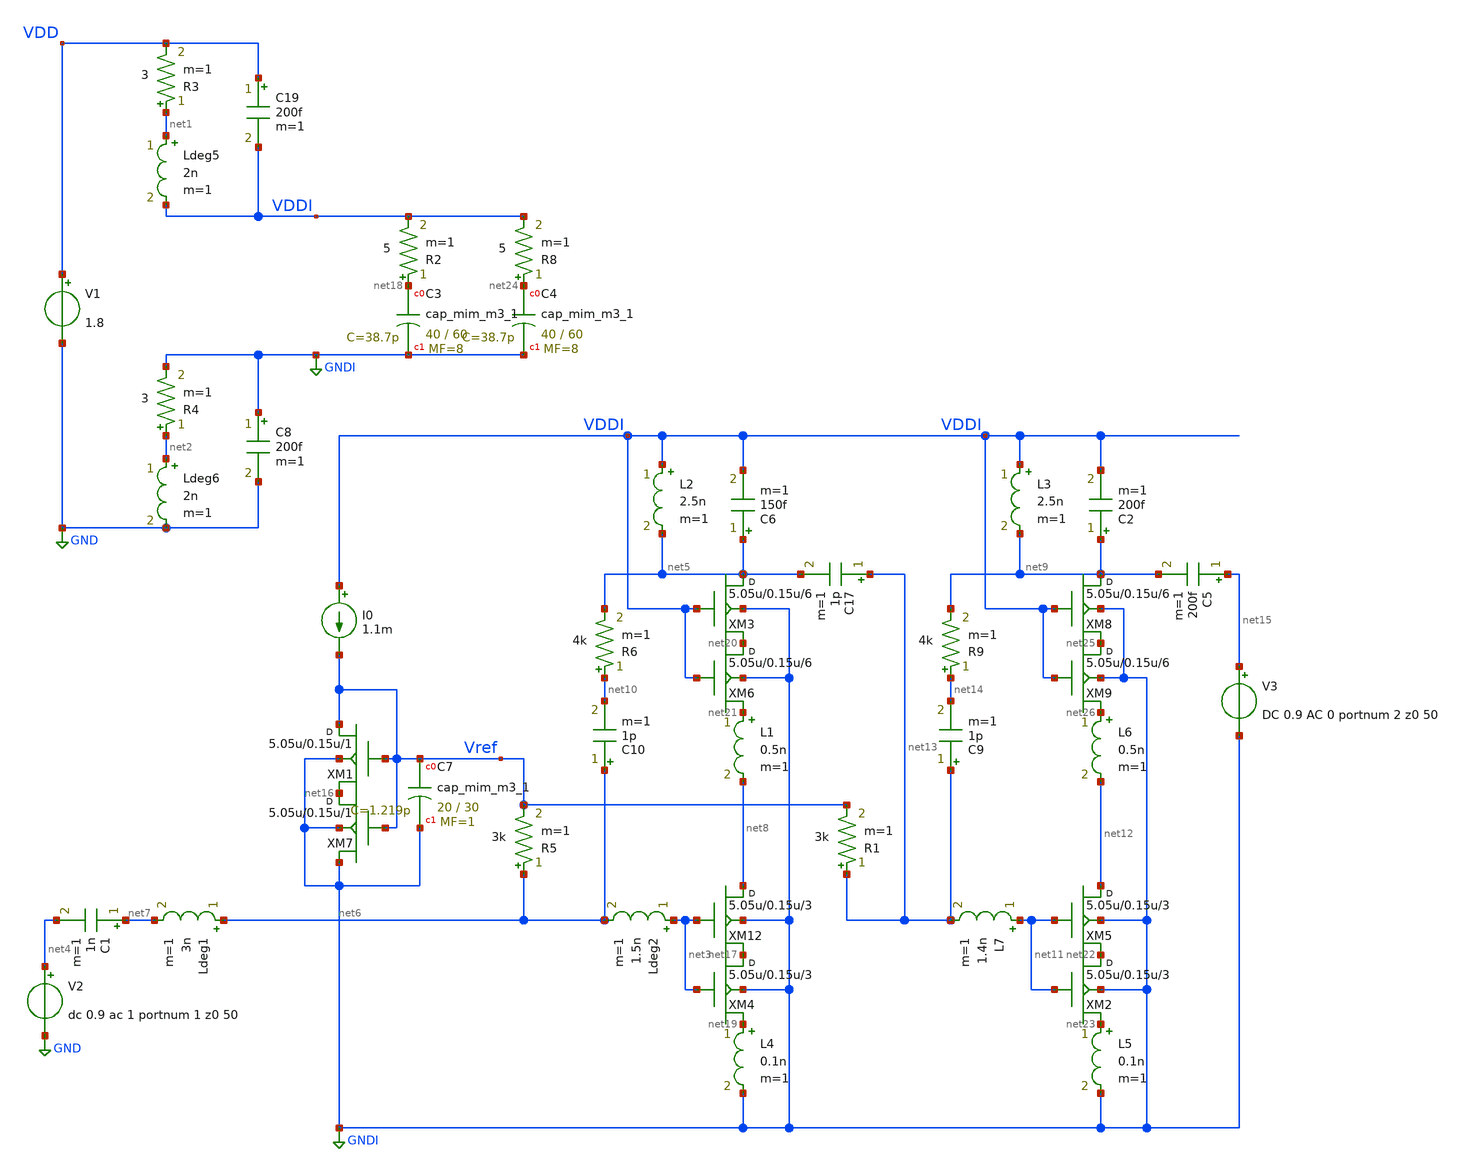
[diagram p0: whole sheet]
** sch_path: xschem/LNA5_with_output_buf_2.sch
**.subckt LNA5_with_output_buf_2
V1 VDD GND 1.8
V2 net4 GND dc 0.9 ac 1 portnum 1 z0 50
I0 VDDI Vref 1.1m
XM1 Vref Vref net16 GNDI sky130_fd_pr__rf_nfet_01v8_bM04W5p00L0p15_ext w=5.05u l=0.15u m=1
XC7 Vref GNDI sky130_fd_pr__cap_mim_m3_1 W=20 L=30 MF=1 m=1
Ldeg5 net1 VDDI 2n m=1
R3 net1 VDD 3 m=1
Ldeg6 net2 GND 2n m=1
R4 net2 GNDI 3 m=1
XM12 net8 net3 net17 GNDI sky130_fd_pr__rf_nfet_01v8_bM04W5p00L0p15_ext w=5.05u l=0.15u m=3
C17 net13 net5 1p m=1
L2 VDDI net5 2.5n m=1
XC3 net18 GNDI sky130_fd_pr__cap_mim_m3_1 W=40 L=60 MF=8 m=8
C8 GNDI GND 200f m=1
C19 VDD VDDI 200f m=1
R2 net18 VDDI 5 m=1
R5 net6 Vref 3k m=1
XM4 net17 net3 net19 GNDI sky130_fd_pr__rf_nfet_01v8_bM04W5p00L0p15_ext w=5.05u l=0.15u m=3
C1 net7 net4 1n m=1
C6 net5 VDDI 150f m=1
R6 net10 net5 4k m=1
XM3 net5 VDDI net20 GNDI sky130_fd_pr__rf_nfet_01v8_bM04W5p00L0p15_ext w=5.05u l=0.15u m=6
XM6 net20 VDDI net21 GNDI sky130_fd_pr__rf_nfet_01v8_bM04W5p00L0p15_ext w=5.05u l=0.15u m=6
XM7 net16 Vref GNDI GNDI sky130_fd_pr__rf_nfet_01v8_bM04W5p00L0p15_ext w=5.05u l=0.15u m=1
Ldeg1 net6 net7 3n m=1
L1 net21 net8 0.5n m=1
Ldeg2 net3 net6 1.5n m=1
XM2 net22 net11 net23 GNDI sky130_fd_pr__rf_nfet_01v8_bM04W5p00L0p15_ext w=5.05u l=0.15u m=3
V3 net15 GNDI DC 0.9 AC 0 portnum 2 z0 50
L5 net23 GNDI 0.1n m=1
L7 net11 net13 1.4n m=1
R1 net13 Vref 3k m=1
XM5 net12 net11 net22 GNDI sky130_fd_pr__rf_nfet_01v8_bM04W5p00L0p15_ext w=5.05u l=0.15u m=3
XC4 net24 GNDI sky130_fd_pr__cap_mim_m3_1 W=40 L=60 MF=8 m=8
R8 net24 VDDI 5 m=1
L3 VDDI net9 2.5n m=1
C2 net9 VDDI 200f m=1
R9 net14 net9 4k m=1
XM8 net9 VDDI net25 GNDI sky130_fd_pr__rf_nfet_01v8_bM04W5p00L0p15_ext w=5.05u l=0.15u m=6
XM9 net25 VDDI net26 GNDI sky130_fd_pr__rf_nfet_01v8_bM04W5p00L0p15_ext w=5.05u l=0.15u m=6
L6 net26 net12 0.5n m=1
C5 net15 net9 200f m=1
C9 net13 net14 1p m=1
C10 net6 net10 1p m=1
L4 net19 GNDI 0.1n m=1
**** begin user architecture code
.lib $::SKYWATER_MODELS/sky130.lib.spice tt
* .include $::PDKPATH/libs.ref/sky130_fd_sc_hvl/spice/sky130_fd_sc_hvl.spice



.subckt sky130_fd_pr__rf_nfet_01v8_bM04W5p00L0p15_ext DRAIN GATE SOURCE SUBSTRATE
X0 DRAIN GATE SOURCE SUBSTRATE sky130_fd_pr__nfet_01v8 ad=2.828e+12p pd=2.132e+07u as=4.242e+12p
+ ps=3.198e+07u w=5.05e+06u l=150000u
X1 SOURCE SUBSTRATE SUBSTRATE SUBSTRATE sky130_fd_pr__nfet_01v8 ad=0p pd=0u as=3.03e+12p
+ ps=2.14e+07u w=5.05e+06u l=150000u
X2 SOURCE GATE DRAIN SUBSTRATE sky130_fd_pr__nfet_01v8 ad=0p pd=0u as=0p ps=0u w=5.05e+06u l=150000u
X3 DRAIN GATE SOURCE SUBSTRATE sky130_fd_pr__nfet_01v8 ad=0p pd=0u as=0p ps=0u w=5.05e+06u l=150000u
X4 SUBSTRATE SUBSTRATE SOURCE SUBSTRATE sky130_fd_pr__nfet_01v8 ad=0p pd=0u as=0p ps=0u w=5.05e+06u
+ l=150000u
X5 SOURCE GATE DRAIN SUBSTRATE sky130_fd_pr__nfet_01v8 ad=0p pd=0u as=0p ps=0u w=5.05e+06u l=150000u
.ends
.sp dec 1000 1e9 10e9 1
* .ac dec 1000 0.01e9 100e9
.control
run
display
let z11=50*(1+s_1_1)/(1-s_1_1)
let z22=50*(1+s_2_2)/(1-s_2_2)
let S11 = S_1_1
let S21 = S_2_1
let S12 = S_1_2
let S22 = S_2_2

* Stability
let delta=S11*S22-S12*S21
let K    = (1-mag(S11)^2-mag(S22)^2+mag(delta)^2)/(2*mag(S12*S21))
let mu   = (1-mag(S11)^2)/(mag(S22-conj(S11)*delta)+mag(S21*S12))
* plot real(z11) real(z22)
* plot imag(z11) imag(z22)
plot db(S_1_1) db(S_2_2) db(S_2_1)

plot db(K)
plot mag(delta)
plot db(mu)
plot NF NFmin
.endc


**** end user architecture code
**.ends
.GLOBAL GND
.GLOBAL GNDI
.end
